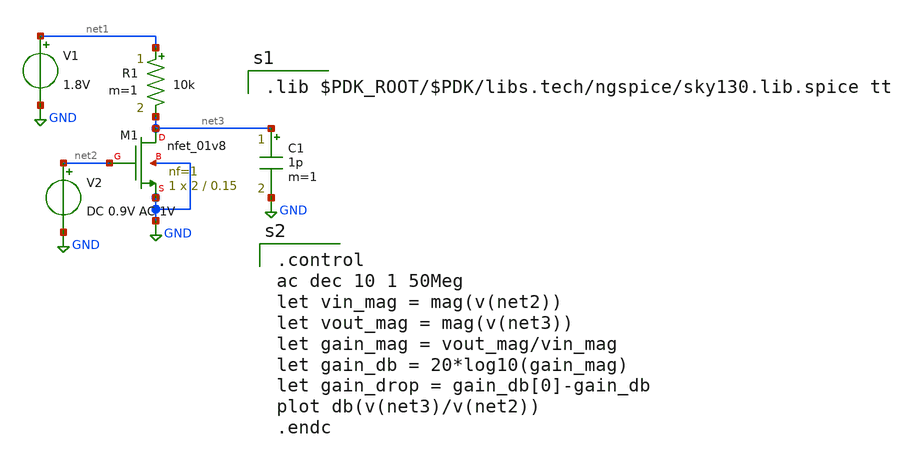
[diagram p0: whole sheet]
** sch_path: schematics/sky130_common_source_amp_cap_test.sch
**.subckt sky130_common_source_amp_cap_test
R1 net1 net3 10k m=1
XM1 net3 net2 GND GND sky130_fd_pr__nfet_01v8 L=0.15 W=2 nf=1 ad='int((nf+1)/2) * W/nf * 0.29' as='int((nf+2)/2) * W/nf * 0.29'
+ pd='2*int((nf+1)/2) * (W/nf + 0.29)' ps='2*int((nf+2)/2) * (W/nf + 0.29)' nrd='0.29 / W' nrs='0.29 / W'
+ sa=0 sb=0 sd=0 mult=1 m=1
V1 net1 GND 1.8V
V2 net2 GND DC 0.9V AC 1V
C1 net3 GND 1p m=1
**** begin user architecture code

.lib $PDK_ROOT/$PDK/libs.tech/ngspice/sky130.lib.spice tt


.control
ac dec 10 1 50Meg
let vin_mag = mag(v(net2))
let vout_mag = mag(v(net3))
let gain_mag = vout_mag/vin_mag
let gain_db = 20*log10(gain_mag)
let gain_drop = gain_db[0]-gain_db
plot db(v(net3)/v(net2))
.endc

**** end user architecture code
**.ends
.GLOBAL GND
.end
